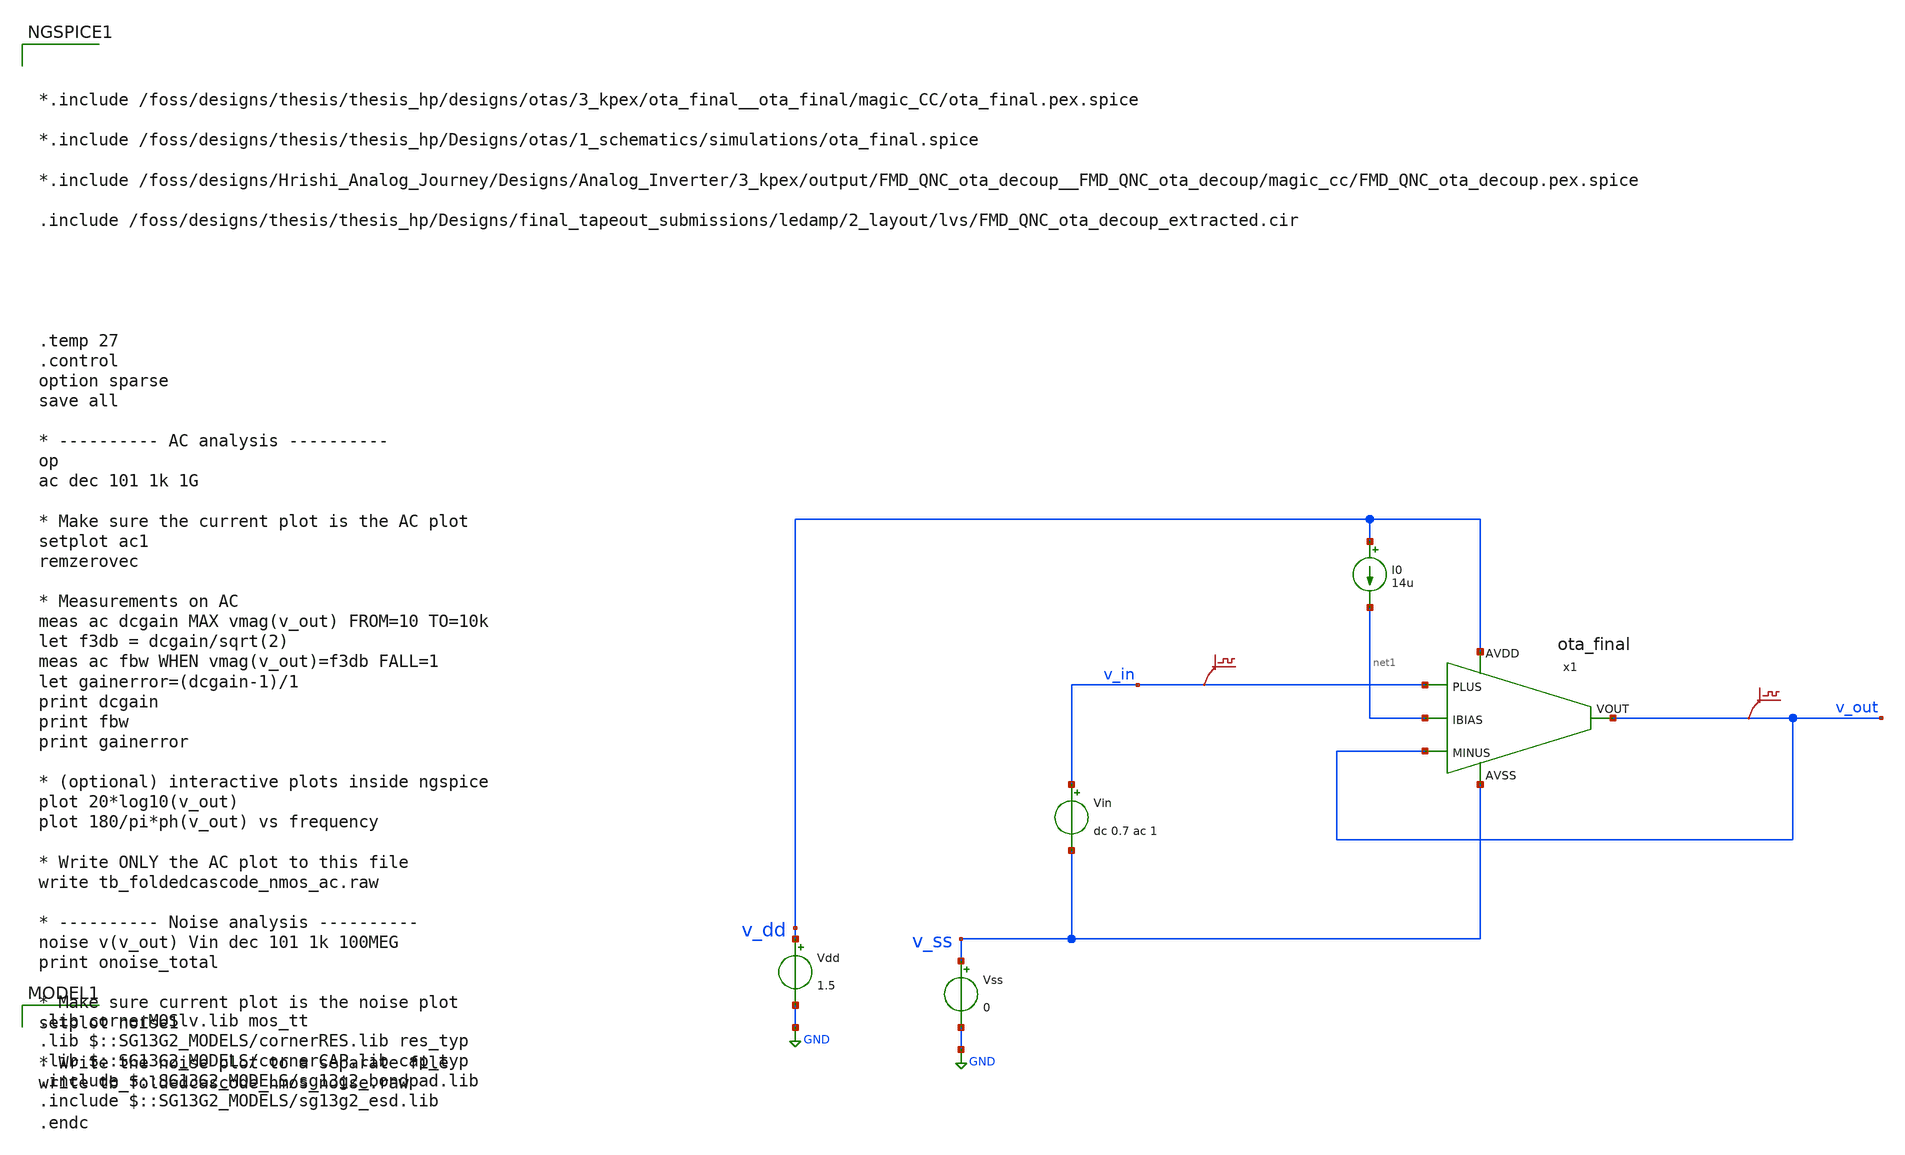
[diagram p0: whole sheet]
** sch_path: Designs/otas/3_kpex/postlayout_testbenches/tb_foldedcascode_nmos_ac.sch
* (c) 2025 Thesis_HP, Apache-2.0 license
**.subckt tb_foldedcascode_nmos_ac
Vss v_ss GND 0
Vdd v_dd GND 1.5
Vin v_in v_ss dc 0.7 ac 1
.save v(v_in)
I0 v_dd net1 14u
.save v(v_out)
x1 v_dd net1 v_out v_out v_in v_ss ota_final
**** begin user architecture code



*.include /foss/designs/thesis/thesis_hp/designs/otas/3_kpex/ota_final__ota_final/magic_CC/ota_final.pex.spice

*.include /foss/designs/thesis/thesis_hp/Designs/otas/1_schematics/simulations/ota_final.spice

*.include /foss/designs/Hrishi_Analog_Journey/Designs/Analog_Inverter/3_kpex/output/FMD_QNC_ota_decoup__FMD_QNC_ota_decoup/magic_cc/FMD_QNC_ota_decoup.pex.spice

.include /foss/designs/thesis/thesis_hp/Designs/final_tapeout_submissions/ledamp/2_layout/lvs/FMD_QNC_ota_decoup_extracted.cir





.temp 27
.control
option sparse
save all

* ---------- AC analysis ----------
op
ac dec 101 1k 1G

* Make sure the current plot is the AC plot
setplot ac1
remzerovec

* Measurements on AC
meas ac dcgain MAX vmag(v_out) FROM=10 TO=10k
let f3db = dcgain/sqrt(2)
meas ac fbw WHEN vmag(v_out)=f3db FALL=1
let gainerror=(dcgain-1)/1
print dcgain
print fbw
print gainerror

* (optional) interactive plots inside ngspice
plot 20*log10(v_out)
plot 180/pi*ph(v_out) vs frequency

* Write ONLY the AC plot to this file
write tb_foldedcascode_nmos_ac.raw

* ---------- Noise analysis ----------
noise v(v_out) Vin dec 101 1k 100MEG
print onoise_total

* Make sure current plot is the noise plot
setplot noise1

* Write the noise plot to a separate file
write tb_foldedcascode_nmos_noise.raw

.endc


 .lib cornerMOSlv.lib mos_tt
.lib $::SG13G2_MODELS/cornerRES.lib res_typ
.lib $::SG13G2_MODELS/cornerCAP.lib cap_typ
.include $::SG13G2_MODELS/sg13g2_bondpad.lib
.include $::SG13G2_MODELS/sg13g2_esd.lib

**** end user architecture code
**.ends
.GLOBAL GND
.end
